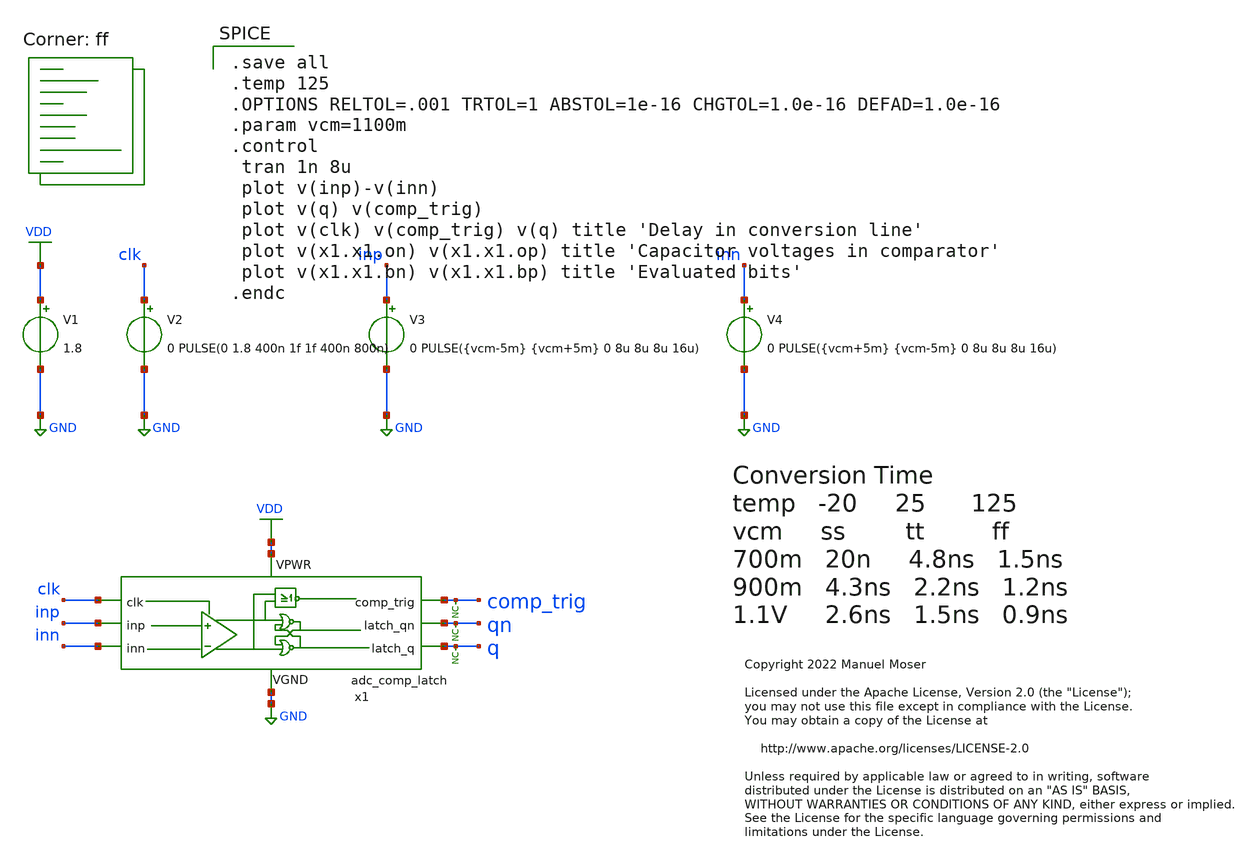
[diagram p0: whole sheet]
** sch_path: xschem/adc_comp_latch_tb.sch
* Copyright 2022 Manuel Moser
* Licensed under the Apache License, Version 2.0 (the "License");
**.subckt adc_comp_latch_tb
V1 VDD GND 1.8
V2 clk GND 0 PULSE(0 1.8 400n 1f 1f 400n 800n)
V3 inp GND 0 PULSE({vcm-5m} {vcm+5m} 0 8u 8u 8u 16u)
V4 inn GND 0 PULSE({vcm+5m} {vcm-5m} 0 8u 8u 8u 16u)
* noconn q
x1 VDD GND clk inp inn comp_trig qn q adc_comp_latch
* noconn comp_trig
* noconn qn
**** begin user architecture code
.lib $::SKYWATER_MODELS/sky130.lib.spice ff

.save all
.temp 125
.OPTIONS RELTOL=.001 TRTOL=1 ABSTOL=1e-16 CHGTOL=1.0e-16 DEFAD=1.0e-16
.param vcm=1100m
.control
 tran 1n 8u
 plot v(inp)-v(inn)
 plot v(q) v(comp_trig)
 plot v(clk) v(comp_trig) v(q) title 'Delay in conversion line'
 plot v(x1.x1.on) v(x1.x1.op) title 'Capacitor voltages in comparator'
 plot v(x1.x1.bn) v(x1.x1.bp) title 'Evaluated bits'
.endc

**** end user architecture code
**.ends
.GLOBAL GND
.GLOBAL VDD
.end
